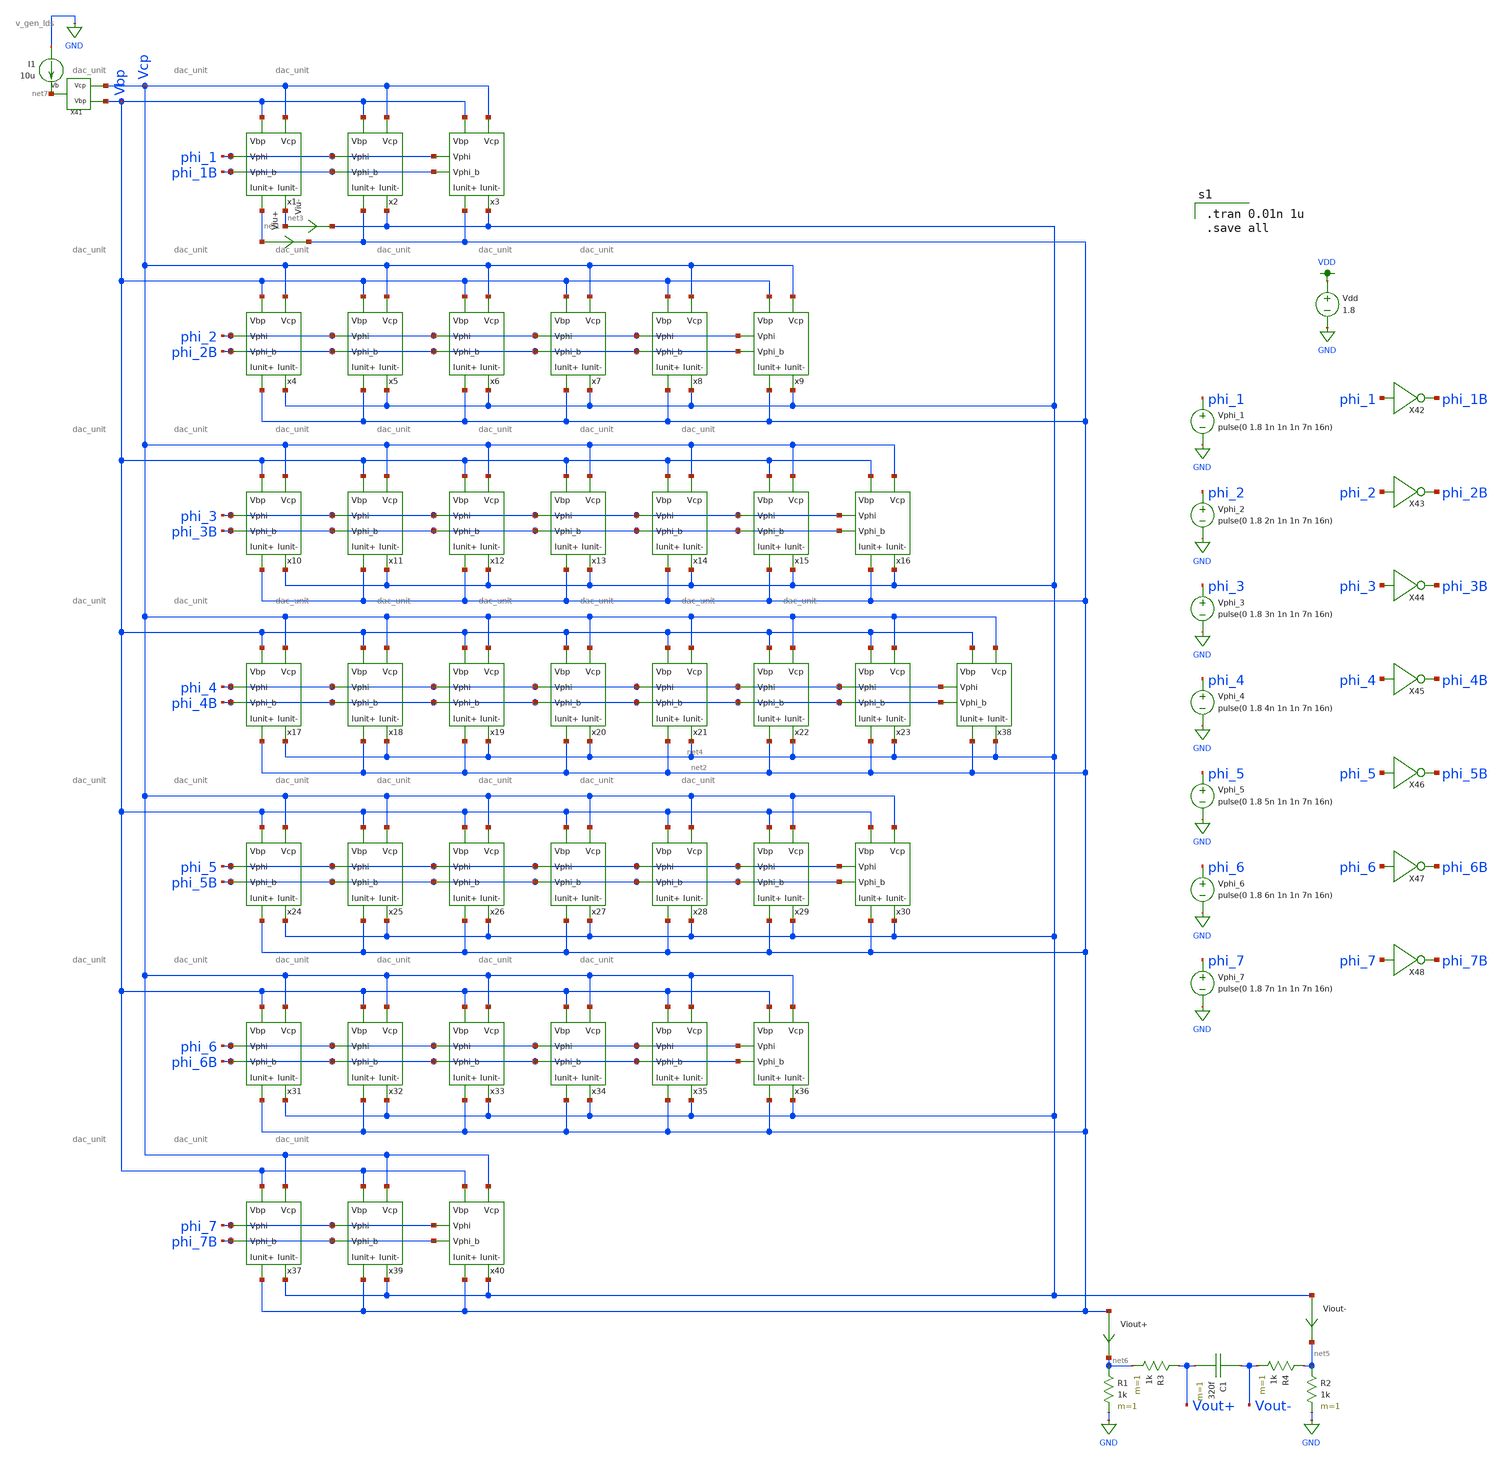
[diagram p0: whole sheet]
** sch_path: simulation/archived/dac_tran.sch
**.subckt dac_tran
x1 Vbp Vcp net1 net3 phi_1 phi_1B dac_unit
x2 Vbp Vcp net2 net4 phi_1 phi_1B dac_unit
x3 Vbp Vcp net2 net4 phi_1 phi_1B dac_unit
x4 Vbp Vcp net2 net4 phi_2 phi_2B dac_unit
x5 Vbp Vcp net2 net4 phi_2 phi_2B dac_unit
x6 Vbp Vcp net2 net4 phi_2 phi_2B dac_unit
x7 Vbp Vcp net2 net4 phi_2 phi_2B dac_unit
x8 Vbp Vcp net2 net4 phi_2 phi_2B dac_unit
x9 Vbp Vcp net2 net4 phi_2 phi_2B dac_unit
x10 Vbp Vcp net2 net4 phi_3 phi_3B dac_unit
x11 Vbp Vcp net2 net4 phi_3 phi_3B dac_unit
x12 Vbp Vcp net2 net4 phi_3 phi_3B dac_unit
x13 Vbp Vcp net2 net4 phi_3 phi_3B dac_unit
x14 Vbp Vcp net2 net4 phi_3 phi_3B dac_unit
x15 Vbp Vcp net2 net4 phi_3 phi_3B dac_unit
x16 Vbp Vcp net2 net4 phi_3 phi_3B dac_unit
x17 Vbp Vcp net2 net4 phi_4 phi_4B dac_unit
x18 Vbp Vcp net2 net4 phi_4 phi_4B dac_unit
x19 Vbp Vcp net2 net4 phi_4 phi_4B dac_unit
x20 Vbp Vcp net2 net4 phi_4 phi_4B dac_unit
x21 Vbp Vcp net2 net4 phi_4 phi_4B dac_unit
x22 Vbp Vcp net2 net4 phi_4 phi_4B dac_unit
x23 Vbp Vcp net2 net4 phi_4 phi_4B dac_unit
x24 Vbp Vcp net2 net4 phi_5 phi_5B dac_unit
x25 Vbp Vcp net2 net4 phi_5 phi_5B dac_unit
x26 Vbp Vcp net2 net4 phi_5 phi_5B dac_unit
x27 Vbp Vcp net2 net4 phi_5 phi_5B dac_unit
x28 Vbp Vcp net2 net4 phi_5 phi_5B dac_unit
x29 Vbp Vcp net2 net4 phi_5 phi_5B dac_unit
x30 Vbp Vcp net2 net4 phi_5 phi_5B dac_unit
x31 Vbp Vcp net2 net4 phi_6 phi_6B dac_unit
x32 Vbp Vcp net2 net4 phi_6 phi_6B dac_unit
x33 Vbp Vcp net2 net4 phi_6 phi_6B dac_unit
x34 Vbp Vcp net2 net4 phi_6 phi_6B dac_unit
x35 Vbp Vcp net2 net4 phi_6 phi_6B dac_unit
x36 Vbp Vcp net2 net4 phi_6 phi_6B dac_unit
x38 Vbp Vcp net2 net4 phi_4 phi_4B dac_unit
x37 Vbp Vcp net2 net4 phi_7 phi_7B dac_unit
x39 Vbp Vcp net2 net4 phi_7 phi_7B dac_unit
x40 Vbp Vcp net2 net4 phi_7 phi_7B dac_unit
X41 Vcp Vbp net7 v_gen_lds
Vdd VDD GND 1.8
Vphi_1 phi_1 GND pulse(0 1.8 1n 1n 1n 7n 16n)
Vphi_2 phi_2 GND pulse(0 1.8 2n 1n 1n 7n 16n)
Vphi_3 phi_3 GND pulse(0 1.8 3n 1n 1n 7n 16n)
Vphi_4 phi_4 GND pulse(0 1.8 4n 1n 1n 7n 16n)
Vphi_5 phi_5 GND pulse(0 1.8 5n 1n 1n 7n 16n)
Vphi_6 phi_6 GND pulse(0 1.8 6n 1n 1n 7n 16n)
Vphi_7 phi_7 GND pulse(0 1.8 7n 1n 1n 7n 16n)
X42 phi_1 phi_1B inverter
X43 phi_2 phi_2B inverter
X44 phi_3 phi_3B inverter
X45 phi_4 phi_4B inverter
X46 phi_5 phi_5B inverter
X47 phi_6 phi_6B inverter
X48 phi_7 phi_7B inverter
R1 net6 GND 1k m=1
R2 net5 GND 1k m=1
R3 Vout+ net6 1k m=1
R4 net5 Vout- 1k m=1
C1 Vout- Vout+ 320f m=1
Viout+ net2 net6 0
.save i(viout+)
Viout- net4 net5 0
.save i(viout-)
I1 GND net7 10u
Viu+ net1 net2 0
.save i(viu+)
Viu- net3 net4 0
.save i(viu-)
**** begin user architecture code

.tran 0.01n 1u
.save all


.option wnflag=1
.param MC_SWITCH=0.0
.lib ~/skywater/skywater-pdk/libraries/sky130_fd_pr_ngspice/latest/models/sky130.lib.spice tt

**** end user architecture code
**.ends
.GLOBAL VDD
.GLOBAL GND
.end
